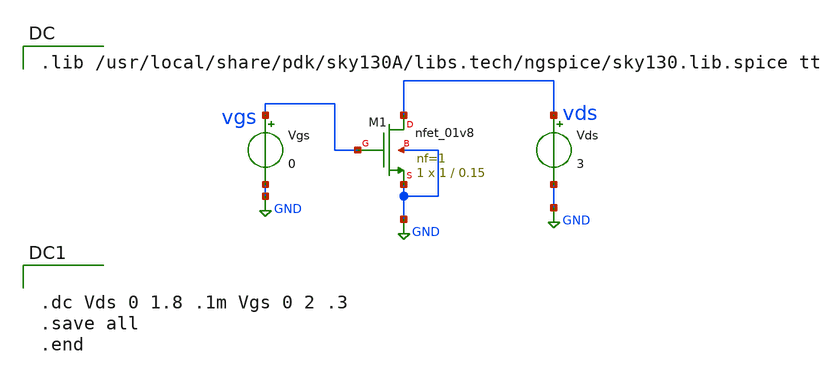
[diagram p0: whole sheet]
** sch_path: Xschem files/dc_sweep.sch
**.subckt dc_sweep
XM1 vds vgs GND GND sky130_fd_pr__nfet_01v8 L=0.15 W=1 nf=1 ad='int((nf+1)/2) * W/nf * 0.29' as='int((nf+2)/2) * W/nf * 0.29'
+ pd='2*int((nf+1)/2) * (W/nf + 0.29)' ps='2*int((nf+2)/2) * (W/nf + 0.29)' nrd='0.29 / W' nrs='0.29 / W'
+ sa=0 sb=0 sd=0 mult=1 m=1
Vgs vgs GND 0
Vds vds GND 3
**** begin user architecture code

.lib /usr/local/share/pdk/sky130A/libs.tech/ngspice/sky130.lib.spice tt



.dc Vds 0 1.8 .1m Vgs 0 2 .3
.save all
.end

**** end user architecture code
**.ends
.GLOBAL GND
.end
